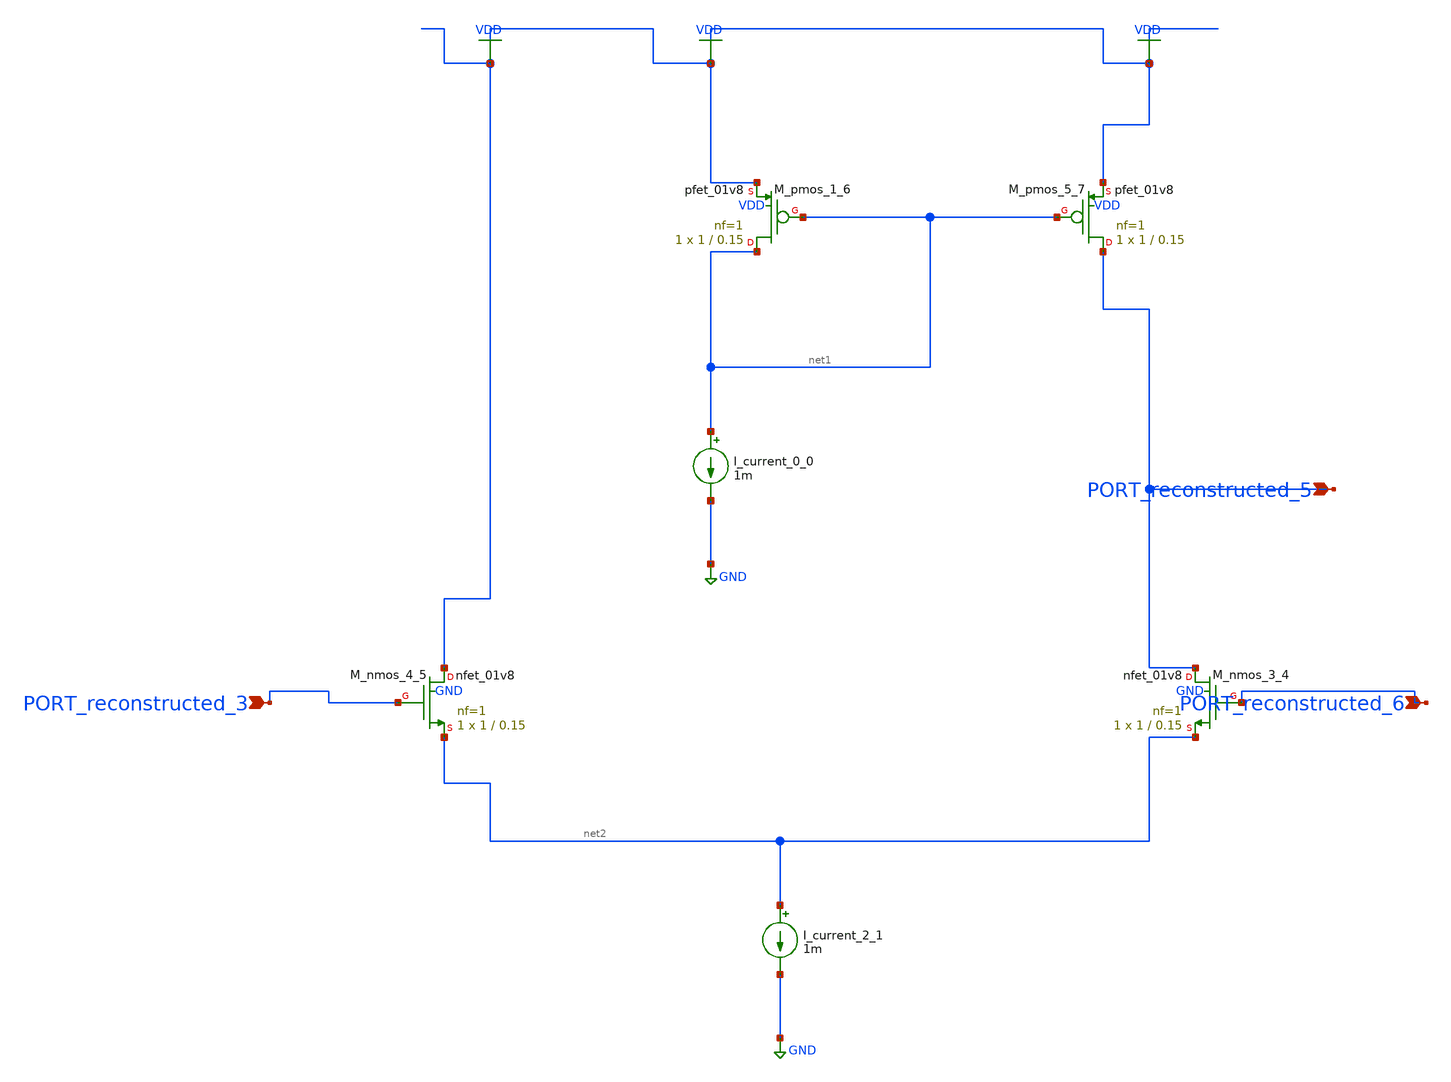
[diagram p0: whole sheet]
** sch_path: schematics/AMSNet/355.sch
**.subckt 355 PORT_reconstructed_3 PORT_reconstructed_5 PORT_reconstructed_6
*.ipin PORT_reconstructed_3
*.ipin PORT_reconstructed_5
*.ipin PORT_reconstructed_6
I_current_0_0 net1 GND 1m
I_current_2_1 net2 GND 1m
XM_nmos_3_4 PORT_reconstructed_5 PORT_reconstructed_6 net2 GND sky130_fd_pr__nfet_01v8 L=0.15 W=1 nf=1
+ ad='int((1 + 1)/2) * 1 / 1 * 0.29' as='int((1 + 2)/2) * 1 / 1 * 0.29' pd='2*int((1 + 1)/2) * (1 / 1 + 0.29)'
+ ps='2*int((1 + 2)/2) * (1 / 1 + 0.29)' nrd='0.29 / 1 ' nrs='0.29 / 1 ' sa=0 sb=0 sd=0 mult=1 m=1
XM_nmos_4_5 VDD PORT_reconstructed_3 net2 GND sky130_fd_pr__nfet_01v8 L=0.15 W=1 nf=1 ad='int((1 + 1)/2) * 1 / 1 * 0.29'
+ as='int((1 + 2)/2) * 1 / 1 * 0.29' pd='2*int((1 + 1)/2) * (1 / 1 + 0.29)' ps='2*int((1 + 2)/2) * (1 / 1 + 0.29)'
+ nrd='0.29 / 1 ' nrs='0.29 / 1 ' sa=0 sb=0 sd=0 mult=1 m=1
XM_pmos_1_6 net1 net1 VDD VDD sky130_fd_pr__pfet_01v8 L=0.15 W=1 nf=1 ad='int((1 + 1)/2) * 1 / 1 * 0.29'
+ as='int((1 + 2)/2) * 1 / 1 * 0.29' pd='2*int((1 + 1)/2) * (1 / 1 + 0.29)' ps='2*int((1 + 2)/2) * (1 / 1 + 0.29)'
+ nrd='0.29 / 1 ' nrs='0.29 / 1 ' sa=0 sb=0 sd=0 mult=1 m=1
XM_pmos_5_7 PORT_reconstructed_5 net1 VDD VDD sky130_fd_pr__pfet_01v8 L=0.15 W=1 nf=1 ad='int((1 + 1)/2) * 1 / 1 * 0.29'
+ as='int((1 + 2)/2) * 1 / 1 * 0.29' pd='2*int((1 + 1)/2) * (1 / 1 + 0.29)' ps='2*int((1 + 2)/2) * (1 / 1 + 0.29)'
+ nrd='0.29 / 1 ' nrs='0.29 / 1 ' sa=0 sb=0 sd=0 mult=1 m=1
**.ends
.GLOBAL GND
.GLOBAL VDD
.end
